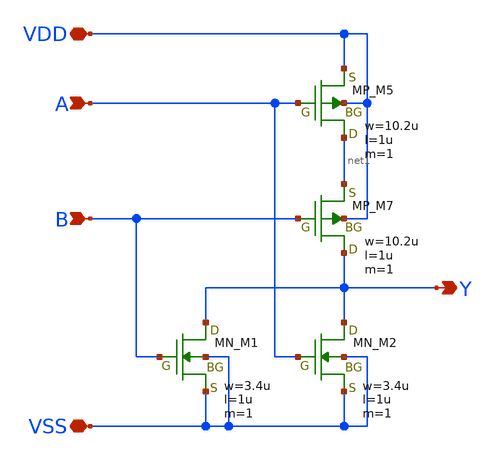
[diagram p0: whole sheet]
** sch_path: member_project/imager/YuMaehashi/design/pulsegen_nor2.sch
**.subckt pulsegen_nor2 A B Y VDD VSS
*.ipin A
*.ipin B
*.opin Y
*.iopin VDD
*.iopin VSS
XM7 Y B net1 VDD PMOS w=10.2u l=1u as=0 ad=0 ps=0 pd=0 nrd=0 nrs=0 m=1
XM1 Y B VSS VSS NMOS w=3.4u l=1u as=0 ad=0 ps=0 pd=0 nrd=0 nrs=0 m=1
XM2 Y A VSS VSS NMOS w=3.4u l=1u as=0 ad=0 ps=0 pd=0 nrd=0 nrs=0 m=1
XM5 net1 A VDD VDD PMOS w=10.2u l=1u as=0 ad=0 ps=0 pd=0 nrd=0 nrs=0 m=1
**.ends
.end
